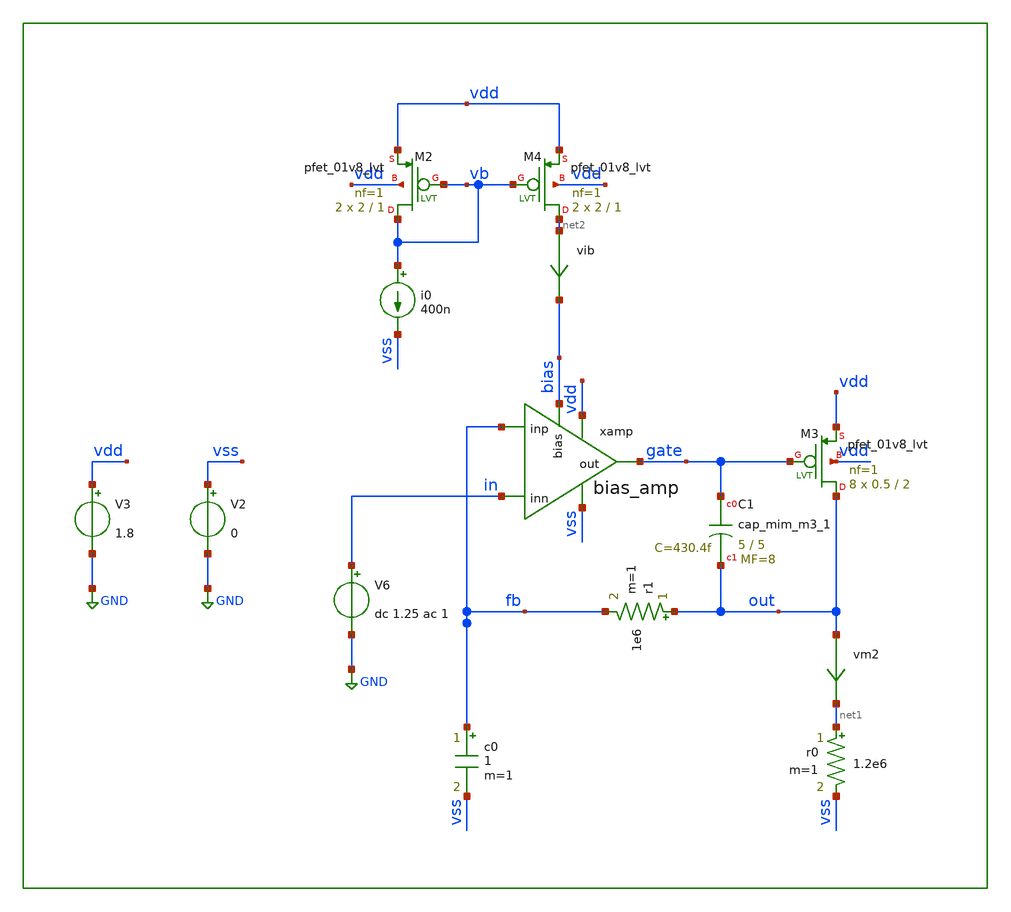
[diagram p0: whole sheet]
** sch_path: xschem/tb/bias/ac_bias_amp.sch
**.subckt ac_bias_amp
V2 vss GND 0
V3 vdd GND 1.8
V6 in GND dc 1.25 ac 1
c0 fb vss 1 m=1
r0 net1 vss 1.2e6 m=1
vm2 out net1 0
.save i(vm2)
xamp vdd gate fb in vss bias bias_amp
r1 out fb 1e6 m=1
XM4 net2 vb vdd vdd sky130_fd_pr__pfet_01v8_lvt L=1 W=2 nf=1 ad='int((nf+1)/2) * W/nf * 0.29' as='int((nf+2)/2) * W/nf * 0.29'
+ pd='2*int((nf+1)/2) * (W/nf + 0.29)' ps='2*int((nf+2)/2) * (W/nf + 0.29)' nrd='0.29 / W' nrs='0.29 / W'
+ sa=0 sb=0 sd=0 mult=2 m=2
i0 vb vss 400n
XM2 vb vb vdd vdd sky130_fd_pr__pfet_01v8_lvt L=1 W=2 nf=1 ad='int((nf+1)/2) * W/nf * 0.29' as='int((nf+2)/2) * W/nf * 0.29'
+ pd='2*int((nf+1)/2) * (W/nf + 0.29)' ps='2*int((nf+2)/2) * (W/nf + 0.29)' nrd='0.29 / W' nrs='0.29 / W'
+ sa=0 sb=0 sd=0 mult=2 m=2
vib net2 bias 0
.save i(vib)
XM3 out gate vdd vdd sky130_fd_pr__pfet_01v8_lvt L=2 W=0.5 nf=1 ad='int((nf+1)/2) * W/nf * 0.29' as='int((nf+2)/2) * W/nf * 0.29'
+ pd='2*int((nf+1)/2) * (W/nf + 0.29)' ps='2*int((nf+2)/2) * (W/nf + 0.29)' nrd='0.29 / W' nrs='0.29 / W'
+ sa=0 sb=0 sd=0 mult=8 m=8
XC1 gate out sky130_fd_pr__cap_mim_m3_1 W=5 L=5 MF=8 m=8
**** begin user architecture code

.control
.param MC_SWITCH=0


* TRAN
* save all
* tran 1n 100u

*AC
save all
op
print all
ac dec 10 100 100e6
let phase=180/3.14*cph(out)
plot vdb(out)
plot phase
let phase=180 + 180/3.14*cph(out)
meas ac ugbw when vdb(out)=0
meas ac pm find phase when vdb(out)=0
.endc



* FET CORNERS
.include $::SKYWATER_MODELS/corners/tt.spice
*.include $::SKYWATER_MODELS/corners/ff.spice
*.include $::SKYWATER_MODELS/corners/ss.spice
*.include $::SKYWATER_MODELS/corners/sf.spice
*.include $::SKYWATER_MODELS/corners/fs.spice

* TT + R + C
*.include $::SKYWATER_MODELS/corners/tt_rmax_cmax.spice
*.include $::SKYWATER_MODELS/corners/tt_rmin_cmin.spice
*.include $::SKYWATER_MODELS/corners/tt_rmax_cmin.spice
*.include $::SKYWATER_MODELS/corners/tt_rmin_cmax.spice

* FF + R + C
*.include $::SKYWATER_MODELS/corners/ff_rmax_cmax.spice
*.include $::SKYWATER_MODELS/corners/ff_rmin_cmin.spice
*.include $::SKYWATER_MODELS/corners/ff_rmax_cmin.spice
*.include $::SKYWATER_MODELS/corners/ff_rmin_cmax.spice


* SS + R + C
*.include $::SKYWATER_MODELS/corners/ss_rmax_cmax.spice
*.include $::SKYWATER_MODELS/corners/ss_rmin_cmin.spice
*.include $::SKYWATER_MODELS/corners/ss_rmax_cmin.spice
*.include $::SKYWATER_MODELS/corners/ss_rmin_cmax.spice

* SF + R + C
*.include $::SKYWATER_MODELS/corners/sf_rmax_cmax.spice
*.include $::SKYWATER_MODELS/corners/sf_rmin_cmin.spice
*.include $::SKYWATER_MODELS/corners/sf_rmax_cmin.spice
*.include $::SKYWATER_MODELS/corners/sf_rmin_cmax.spice

* FS + R + C
*.include $::SKYWATER_MODELS/corners/fs_rmax_cmax.spice
*.include $::SKYWATER_MODELS/corners/fs_rmin_cmin.spice
*.include $::SKYWATER_MODELS/corners/fs_rmax_cmin.spice
*.include $::SKYWATER_MODELS/corners/fs_rmin_cmax.spice

**** end user architecture code
**.ends

* expanding   symbol:  bias/bias_amp.sym # of pins=6
** sym_path: xschem/bias/bias_amp.sym
** sch_path: xschem/bias/bias_amp.sch
.subckt bias_amp vdd out inp inn vss bias
*.iopin vdd
*.iopin bias
*.ipin inp
*.ipin inn
*.opin out
*.iopin vss
XM3 mirr mirr vdd vdd sky130_fd_pr__pfet_01v8_lvt L=10 W=0.5 nf=1 ad='int((nf+1)/2) * W/nf * 0.29' as='int((nf+2)/2) * W/nf * 0.29'
+ pd='2*int((nf+1)/2) * (W/nf + 0.29)' ps='2*int((nf+2)/2) * (W/nf + 0.29)' nrd='0.29 / W' nrs='0.29 / W'
+ sa=0 sb=0 sd=0 mult=4 m=4
XM4 out mirr vdd vdd sky130_fd_pr__pfet_01v8_lvt L=10 W=0.5 nf=1 ad='int((nf+1)/2) * W/nf * 0.29' as='int((nf+2)/2) * W/nf * 0.29'
+ pd='2*int((nf+1)/2) * (W/nf + 0.29)' ps='2*int((nf+2)/2) * (W/nf + 0.29)' nrd='0.29 / W' nrs='0.29 / W'
+ sa=0 sb=0 sd=0 mult=4 m=4
XM1 mirr inp diff vss sky130_fd_pr__nfet_01v8_lvt L=8 W=0.5 nf=1 ad='int((nf+1)/2) * W/nf * 0.29' as='int((nf+2)/2) * W/nf * 0.29'
+ pd='2*int((nf+1)/2) * (W/nf + 0.29)' ps='2*int((nf+2)/2) * (W/nf + 0.29)' nrd='0.29 / W' nrs='0.29 / W'
+ sa=0 sb=0 sd=0 mult=4 m=4
XM2 out inn diff vss sky130_fd_pr__nfet_01v8_lvt L=8 W=0.5 nf=1 ad='int((nf+1)/2) * W/nf * 0.29' as='int((nf+2)/2) * W/nf * 0.29'
+ pd='2*int((nf+1)/2) * (W/nf + 0.29)' ps='2*int((nf+2)/2) * (W/nf + 0.29)' nrd='0.29 / W' nrs='0.29 / W'
+ sa=0 sb=0 sd=0 mult=4 m=4
XM5 net1 bias vss vss sky130_fd_pr__nfet_01v8_lvt L=4 W=0.5 nf=1 ad='int((nf+1)/2) * W/nf * 0.29' as='int((nf+2)/2) * W/nf * 0.29'
+ pd='2*int((nf+1)/2) * (W/nf + 0.29)' ps='2*int((nf+2)/2) * (W/nf + 0.29)' nrd='0.29 / W' nrs='0.29 / W'
+ sa=0 sb=0 sd=0 mult=4 m=4
XM6 bias bias vss vss sky130_fd_pr__nfet_01v8_lvt L=4 W=0.5 nf=1 ad='int((nf+1)/2) * W/nf * 0.29' as='int((nf+2)/2) * W/nf * 0.29'
+ pd='2*int((nf+1)/2) * (W/nf + 0.29)' ps='2*int((nf+2)/2) * (W/nf + 0.29)' nrd='0.29 / W' nrs='0.29 / W'
+ sa=0 sb=0 sd=0 mult=8 m=8
XM5s diff bias net1 vss sky130_fd_pr__nfet_01v8_lvt L=4 W=0.5 nf=1 ad='int((nf+1)/2) * W/nf * 0.29' as='int((nf+2)/2) * W/nf * 0.29'
+ pd='2*int((nf+1)/2) * (W/nf + 0.29)' ps='2*int((nf+2)/2) * (W/nf + 0.29)' nrd='0.29 / W' nrs='0.29 / W'
+ sa=0 sb=0 sd=0 mult=4 m=4
.ends

.GLOBAL GND
.end
